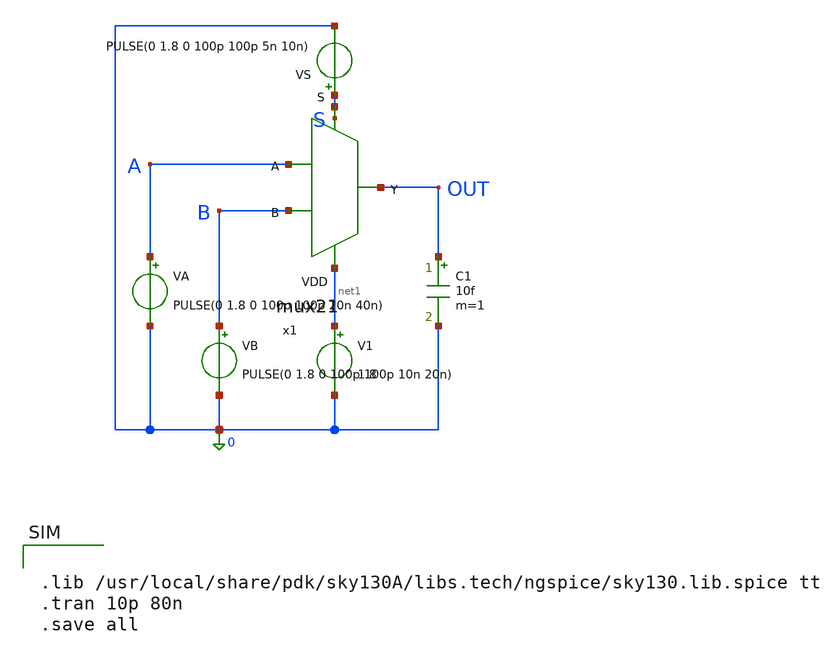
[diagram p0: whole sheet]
** sch_path: testbench/mux21_tb.sch
**.subckt mux21_tb
VA A 0 PULSE(0 1.8 0 100p 100p 20n 40n)
VB B 0 PULSE(0 1.8 0 100p 100p 10n 20n)
VS S 0 PULSE(0 1.8 0 100p 100p 5n 10n)
C1 OUT 0 10f m=1
V1 net1 0 1.8
x1 A S OUT B net1 mux21
**** begin user architecture code


.lib /usr/local/share/pdk/sky130A/libs.tech/ngspice/sky130.lib.spice tt
.tran 10p 80n
.save all


**** end user architecture code
**.ends
.end
